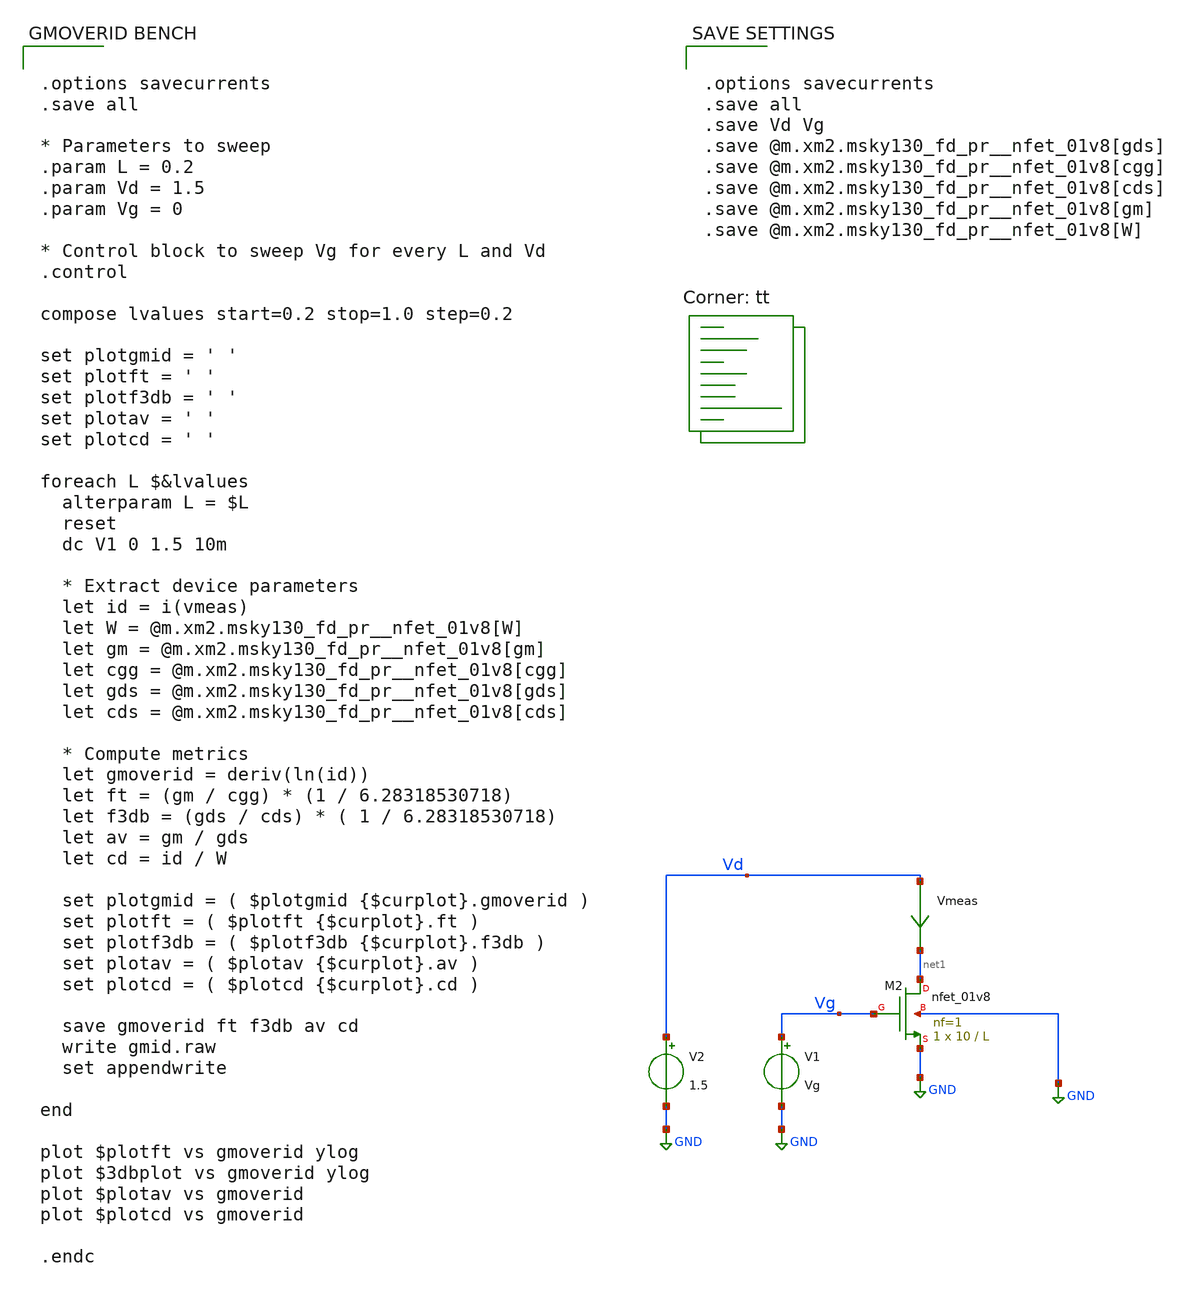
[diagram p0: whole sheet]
** sch_path: gmid.sch
**.subckt gmid
V1 Vg GND Vg
V2 Vd GND 1.5
XM2 net1 Vg GND GND sky130_fd_pr__nfet_01v8 L=L W=10 nf=1 ad='int((1 + 1)/2) * 10 / 1 * 0.29' as='int((1 + 2)/2) * 10 / 1 * 0.29'
+ pd='2*int((1 + 1)/2) * (10 / 1 + 0.29)' ps='2*int((1 + 2)/2) * (10 / 1 + 0.29)' nrd='0.29 / 10 ' nrs='0.29 / 10 '
+ sa=0 sb=0 sd=0 mult=1 m=1
Vmeas Vd net1 0
.save i(vmeas)
**** begin user architecture code
.lib $::SKYWATER_MODELS/sky130.lib.spice tt


.options savecurrents
.save all

* Parameters to sweep
.param L = 0.2
.param Vd = 1.5
.param Vg = 0

* Control block to sweep Vg for every L and Vd
.control

compose lvalues start=0.2 stop=1.0 step=0.2

set plotgmid = ' '
set plotft = ' '
set plotf3db = ' '
set plotav = ' '
set plotcd = ' '

foreach L $&lvalues
  alterparam L = $L
  reset
  dc V1 0 1.5 10m

  * Extract device parameters
  let id = i(vmeas)
  let W = @m.xm2.msky130_fd_pr__nfet_01v8[W]
  let gm = @m.xm2.msky130_fd_pr__nfet_01v8[gm]
  let cgg = @m.xm2.msky130_fd_pr__nfet_01v8[cgg]
  let gds = @m.xm2.msky130_fd_pr__nfet_01v8[gds]
  let cds = @m.xm2.msky130_fd_pr__nfet_01v8[cds]

  * Compute metrics
  let gmoverid = deriv(ln(id))
  let ft = (gm / cgg) * (1 / 6.28318530718)
  let f3db = (gds / cds) * ( 1 / 6.28318530718)
  let av = gm / gds
  let cd = id / W

  set plotgmid = ( $plotgmid {$curplot}.gmoverid )
  set plotft = ( $plotft {$curplot}.ft )
  set plotf3db = ( $plotf3db {$curplot}.f3db )
  set plotav = ( $plotav {$curplot}.av )
  set plotcd = ( $plotcd {$curplot}.cd )

  save gmoverid ft f3db av cd
  write gmid.raw
  set appendwrite

end

plot $plotft vs gmoverid ylog
plot $3dbplot vs gmoverid ylog
plot $plotav vs gmoverid
plot $plotcd vs gmoverid

.endc




.options savecurrents
.save all
.save Vd Vg
.save @m.xm2.msky130_fd_pr__nfet_01v8[gds]
.save @m.xm2.msky130_fd_pr__nfet_01v8[cgg]
.save @m.xm2.msky130_fd_pr__nfet_01v8[cds]
.save @m.xm2.msky130_fd_pr__nfet_01v8[gm]
.save @m.xm2.msky130_fd_pr__nfet_01v8[W]


**** end user architecture code
**.ends
.GLOBAL GND
.end
